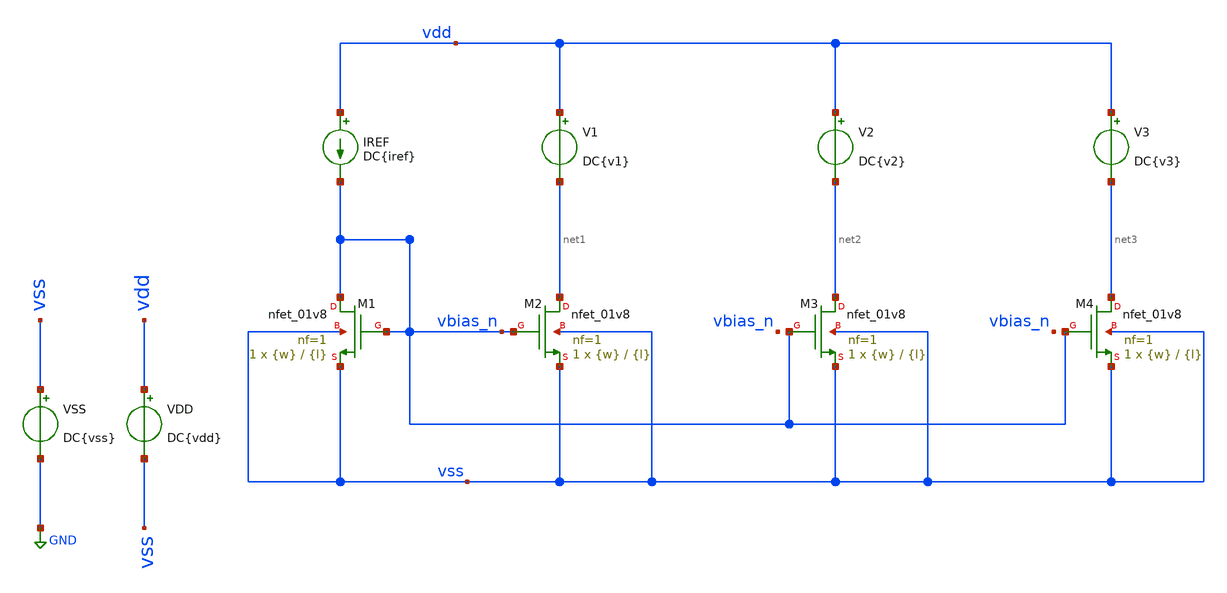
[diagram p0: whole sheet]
** sch_path: Tp2/Mis Simulaciones/tp2_2.sch
**.subckt tp2_2
XM1 vbias_n vbias_n vss vss sky130_fd_pr__nfet_01v8 L={l} W={w} nf=1 ad='int((nf+1)/2) * W/nf * 0.29'
+ as='int((nf+2)/2) * W/nf * 0.29' pd='2*int((nf+1)/2) * (W/nf + 0.29)' ps='2*int((nf+2)/2) * (W/nf + 0.29)'
+ nrd='0.29 / W' nrs='0.29 / W' sa=0 sb=0 sd=0 mult=1 m=1
XM2 net1 vbias_n vss vss sky130_fd_pr__nfet_01v8 L={l} W={w} nf=1 ad='int((nf+1)/2) * W/nf * 0.29' as='int((nf+2)/2) * W/nf * 0.29'
+ pd='2*int((nf+1)/2) * (W/nf + 0.29)' ps='2*int((nf+2)/2) * (W/nf + 0.29)' nrd='0.29 / W' nrs='0.29 / W'
+ sa=0 sb=0 sd=0 mult=1 m=1
IREF vdd vbias_n DC{iref}
VSS vss GND DC{vss}
VDD vdd vss DC{vdd}
XM3 net2 vbias_n vss vss sky130_fd_pr__nfet_01v8 L={l} W={w} nf=1 ad='int((nf+1)/2) * W/nf * 0.29' as='int((nf+2)/2) * W/nf * 0.29'
+ pd='2*int((nf+1)/2) * (W/nf + 0.29)' ps='2*int((nf+2)/2) * (W/nf + 0.29)' nrd='0.29 / W' nrs='0.29 / W'
+ sa=0 sb=0 sd=0 mult=1 m=1
XM4 net3 vbias_n vss vss sky130_fd_pr__nfet_01v8 L={l} W={w} nf=1 ad='int((nf+1)/2) * W/nf * 0.29' as='int((nf+2)/2) * W/nf * 0.29'
+ pd='2*int((nf+1)/2) * (W/nf + 0.29)' ps='2*int((nf+2)/2) * (W/nf + 0.29)' nrd='0.29 / W' nrs='0.29 / W'
+ sa=0 sb=0 sd=0 mult=1 m=1
V2 vdd net2 DC{v2}
V3 vdd net3 DC{v3}
V1 vdd net1 DC{v1}
**** begin user architecture code



* Parameters
.param vdd = 1.8
.param vss = 0.0
.param iref = 200u
.param w = 4.2
.param l = 0.15
.param v1 = 0.6
.param v2 = 0.9
.param v3 = 1.2
.options TEMPS = 27.0

* Models
.lib ~/skywater/skywater-pdk/libraries/sky130_fd_pr_ngspice/latest/models/corners/sky130.lib TT

* Data to save
.save all  @M.XM1.msky130_fd_pr__nfet_01v8[id]  @M.XM1.msky130_fd_pr__nfet_01v8[vth]  @M.XM1.msky130_fd_pr__nfet_01v8[vdsat]  @M.XM1.msky130_fd_pr__nfet_01v8[gm]  @M.XM1.msky130_fd_pr__nfet_01v8[vds]  @M.XM1.msky130_fd_pr__nfet_01v8[vgs]  @M.XM1.msky130_fd_pr__nfet_01v8[w]  @M.XM2.msky130_fd_pr__nfet_01v8[id]  @M.XM2.msky130_fd_pr__nfet_01v8[vth]  @M.XM2.msky130_fd_pr__nfet_01v8[gm]  @M.XM2.msky130_fd_pr__nfet_01v8[vds]  @M.XM2.msky130_fd_pr__nfet_01v8[vgs]  @M.XM2.msky130_fd_pr__nfet_01v8[w]  @M.XM3.msky130_fd_pr__nfet_01v8[id]  @M.XM3.msky130_fd_pr__nfet_01v8[vth]  @M.XM3.msky130_fd_pr__nfet_01v8[gm]  @M.XM3.msky130_fd_pr__nfet_01v8[vds]  @M.XM3.msky130_fd_pr__nfet_01v8[vgs]  @M.XM3.msky130_fd_pr__nfet_01v8[w]  @M.XM4.msky130_fd_pr__nfet_01v8[id]  @M.XM4.msky130_fd_pr__nfet_01v8[vth]  @M.XM4.msky130_fd_pr__nfet_01v8[gm]  @M.XM4.msky130_fd_pr__nfet_01v8[vds]  @M.XM4.msky130_fd_pr__nfet_01v8[vgs]  @M.XM4.msky130_fd_pr__nfet_01v8[w]

* Simulation
.control
  *let wi = 1.5
  *let wf = 4.5
  *let wstep = 0.15

  *dowhile wi <= wf
    *print @M.XM1.msky130_fd_pr__nfet_01v8[w]
    *alter @M.XM1.msky130_fd_pr__nfet_01v8[w] = wi
    *alter @M.XM2.msky130_fd_pr__nfet_01v8[w] = wi
    *let wi = wi + wstep
    *op
    *print @M.XM1.msky130_fd_pr__nfet_01v8[w]
    *print @M.XM1.msky130_fd_pr__nfet_01v8[id]
    *print @M.XM1.msky130_fd_pr__nfet_01v8[vds]
    *print @M.XM1.msky130_fd_pr__nfet_01v8[vgs]
    *print @M.XM2.msky130_fd_pr__nfet_01v8[w]
    *print @M.XM2.msky130_fd_pr__nfet_01v8[id]
    *print @M.XM2.msky130_fd_pr__nfet_01v8[vds]
    *print @M.XM2.msky130_fd_pr__nfet_01v8[vgs]
    *print @M.XM3.msky130_fd_pr__nfet_01v8[w]
    *print @M.XM3.msky130_fd_pr__nfet_01v8[id]
    *print @M.XM3.msky130_fd_pr__nfet_01v8[vds]
    *print @M.XM3.msky130_fd_pr__nfet_01v8[vgs]
    *print @M.XM4.msky130_fd_pr__nfet_01v8[w]
    *print @M.XM4.msky130_fd_pr__nfet_01v8[id]
    *print @M.XM4.msky130_fd_pr__nfet_01v8[vds]
    *print @M.XM4.msky130_fd_pr__nfet_01v8[vgs]
    *save all
  *end
  *write tp2_2.raw


  unset filetype
  op
  save all
  write tp2_2.raw

.endc

.end


**** end user architecture code
**.ends
.GLOBAL GND
.end
